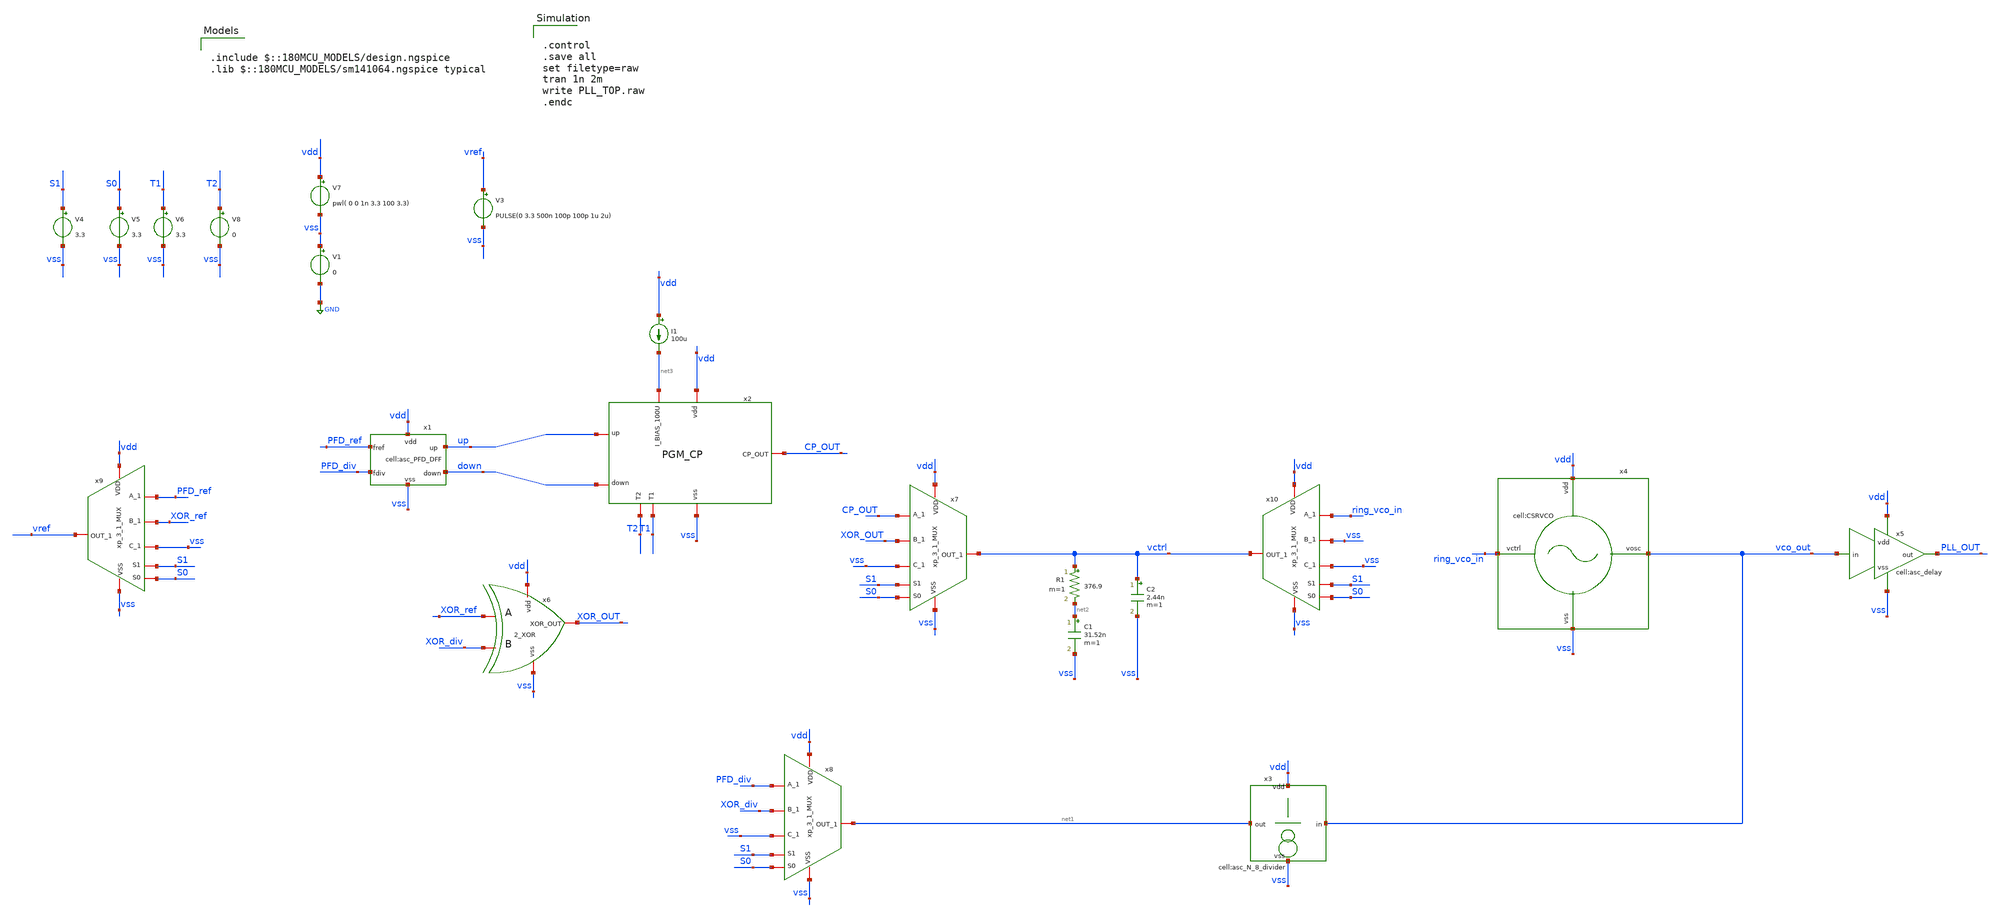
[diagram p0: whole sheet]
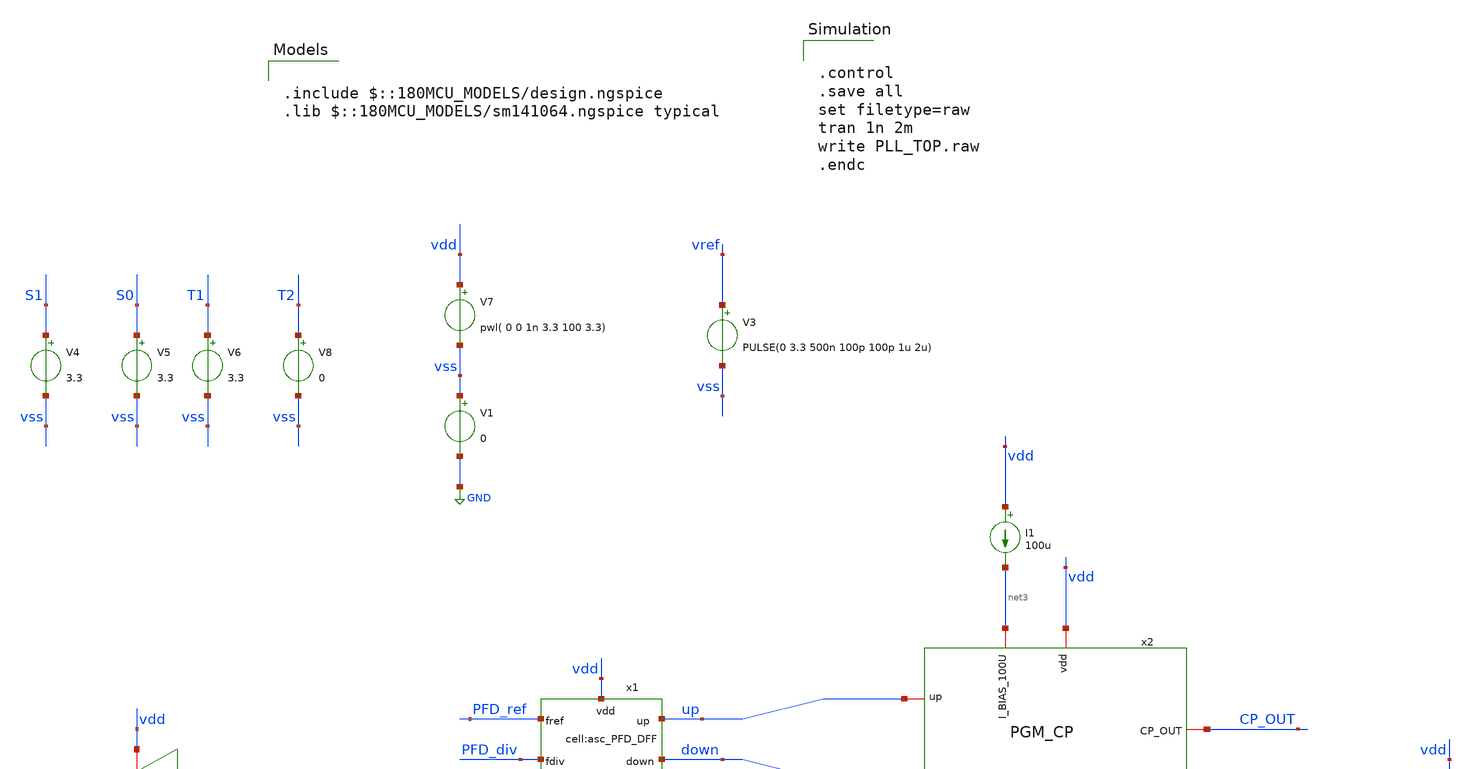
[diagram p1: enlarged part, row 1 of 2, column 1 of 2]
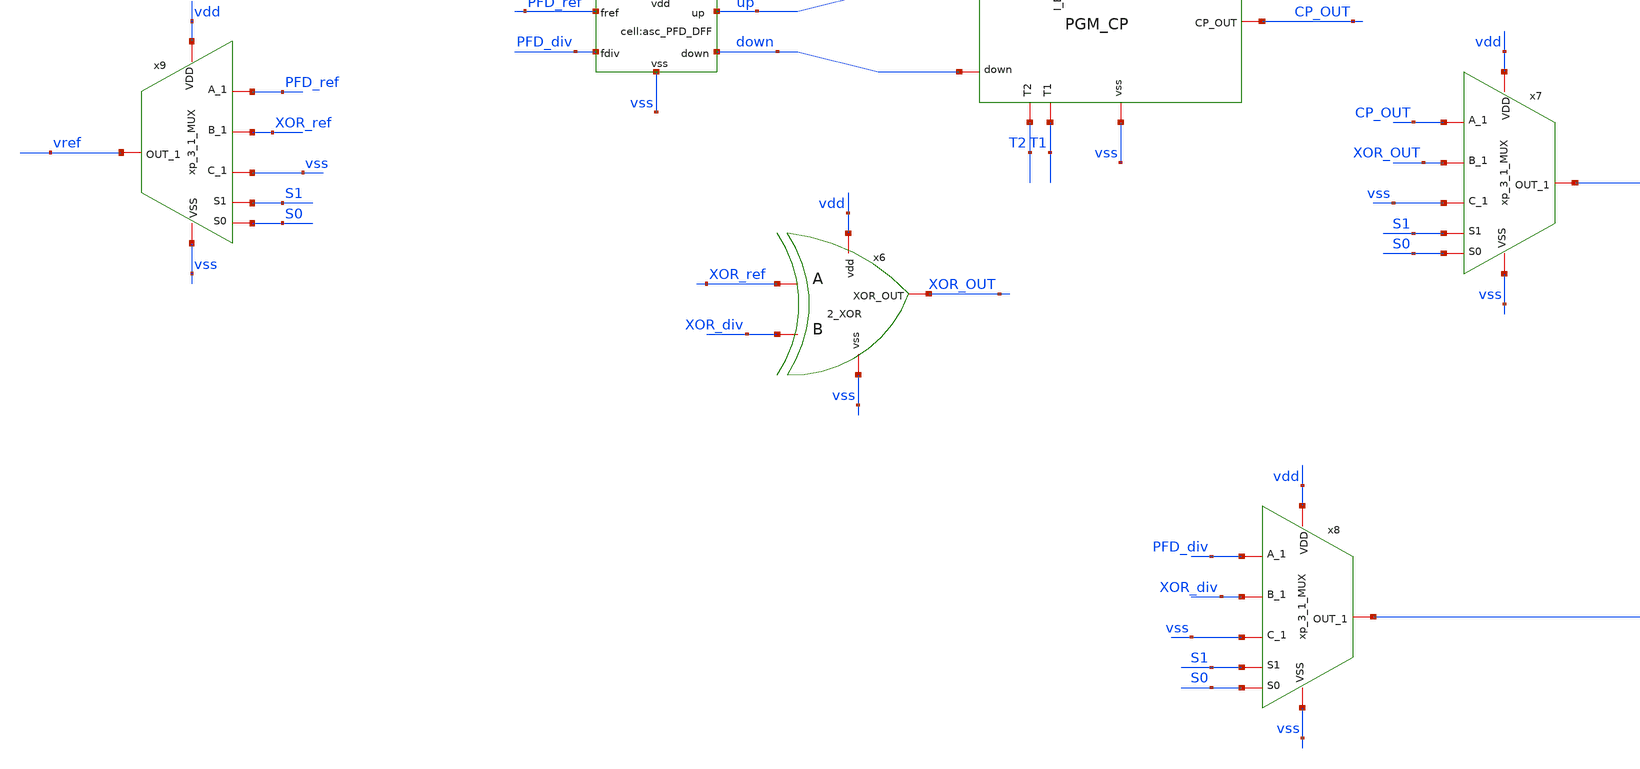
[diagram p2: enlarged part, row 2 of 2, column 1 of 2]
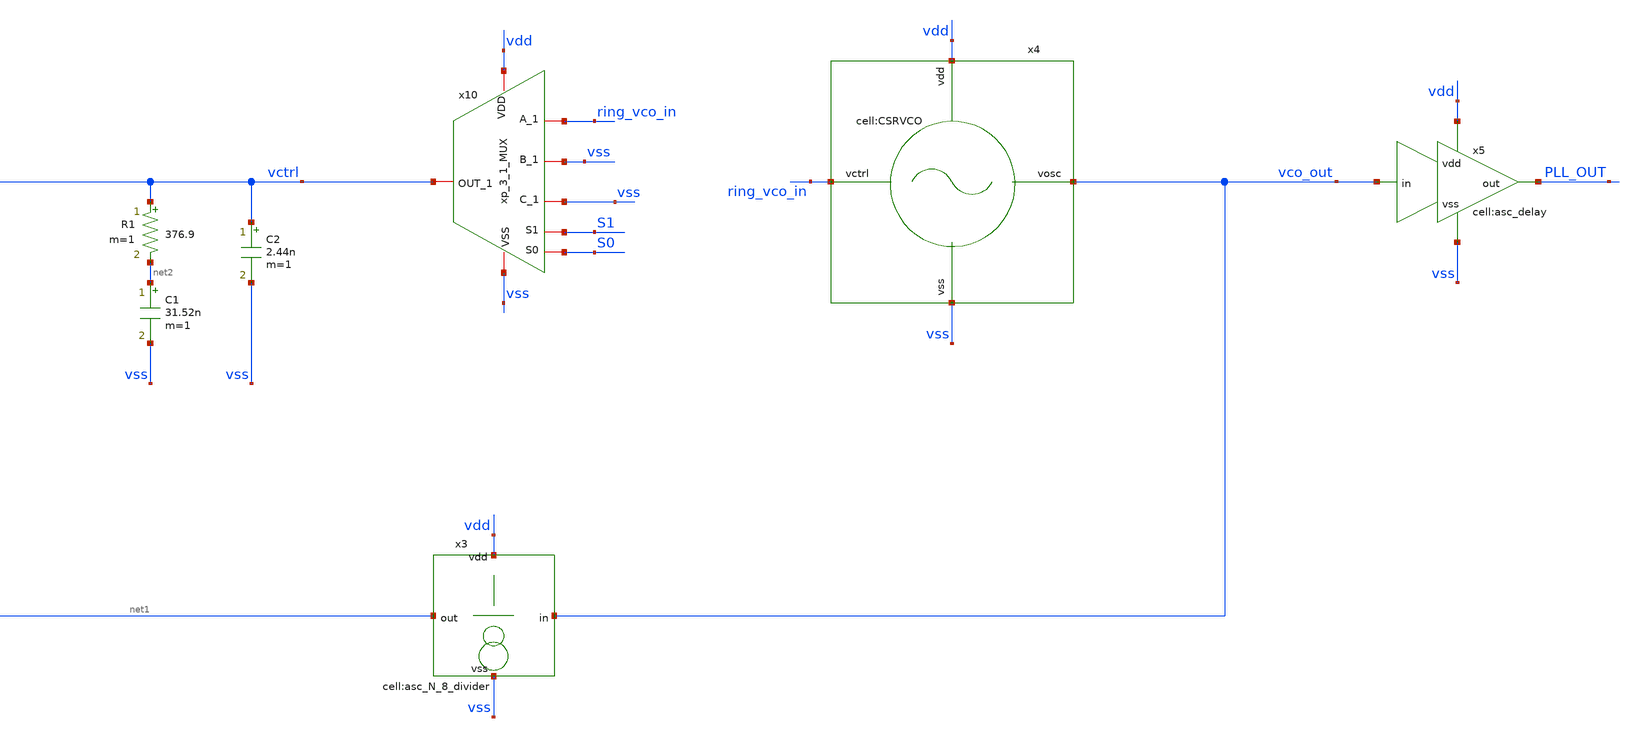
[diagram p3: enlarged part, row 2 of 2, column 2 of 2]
** sch_path: designs/libs/tb_analog/PGM_PLL_TOP.sch
**.subckt PGM_PLL_TOP
V1 vss GND 0
V3 vref vss PULSE(0 3.3 500n 100p 100p 1u 2u)
x1 vdd vss down up PFD_ref PFD_div asc_PFD_DFF
x3 vco_out net1 vdd vss asc_N_8_divider
x4 ring_vco_in vdd vss vco_out CSRVCO
x5 vco_out vss PLL_OUT vdd asc_delay
C1 net2 vss 31.52n m=1
C2 vctrl vss 2.44n m=1
R1 vctrl net2 376.9 m=1
I1 vdd net3 100u
x2 vdd CP_OUT vss T1 T2 up down net3 PGM_CP
V6 T1 vss 3.3
V8 T2 vss 0
x7 CP_OUT vdd vss S0 S1 XOR_OUT vctrl vss xp_3_1_MUX
x6 XOR_ref XOR_div vss vdd XOR_OUT 2_XOR
V4 S1 vss 3.3
V5 S0 vss 3.3
x8 PFD_div vdd vss S0 S1 XOR_div net1 vss xp_3_1_MUX
x9 PFD_ref vdd vss S0 S1 XOR_ref vref vss xp_3_1_MUX
x10 ring_vco_in vdd vss S0 S1 vss vctrl vss xp_3_1_MUX
V7 vdd vss pwl( 0 0 1n 3.3 100 3.3)
**** begin user architecture code

.include $::180MCU_MODELS/design.ngspice
.lib $::180MCU_MODELS/sm141064.ngspice typical



.control
.save all
set filetype=raw
tran 1n 2m
write PLL_TOP.raw
.endc


**** end user architecture code
**.ends
.GLOBAL GND
.end
